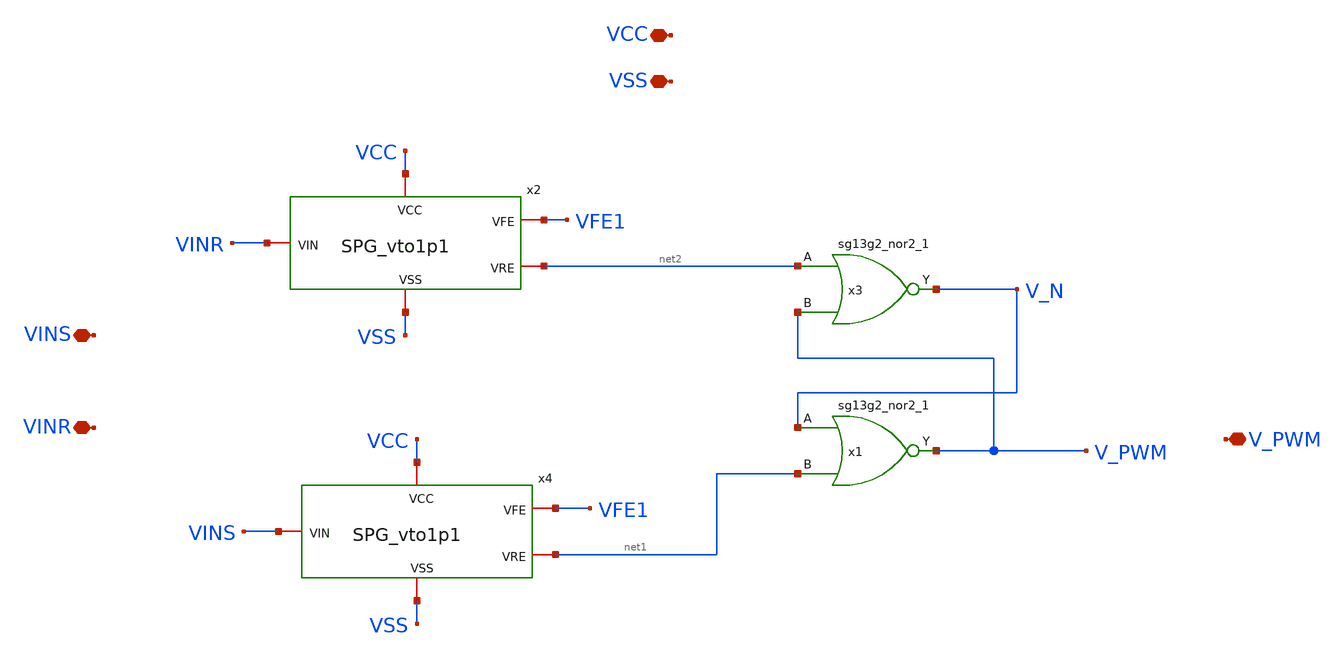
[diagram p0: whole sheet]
** sch_path: xschem/PD_vto1p1.sch
**.subckt PD_vto1p1 V_PWM VCC VSS VINS VINR
*.iopin V_PWM
*.iopin VCC
*.iopin VSS
*.iopin VINS
*.iopin VINR
x3 V_N net2 V_PWM VCC VSS sg13g2_nor2_1
x1 V_PWM V_N net1 VCC VSS sg13g2_nor2_1
x2 VCC VSS VFE1 VINR net2 SPG_vto1p1
x4 VCC VSS VFE1 VINS net1 SPG_vto1p1
**.ends
.end
